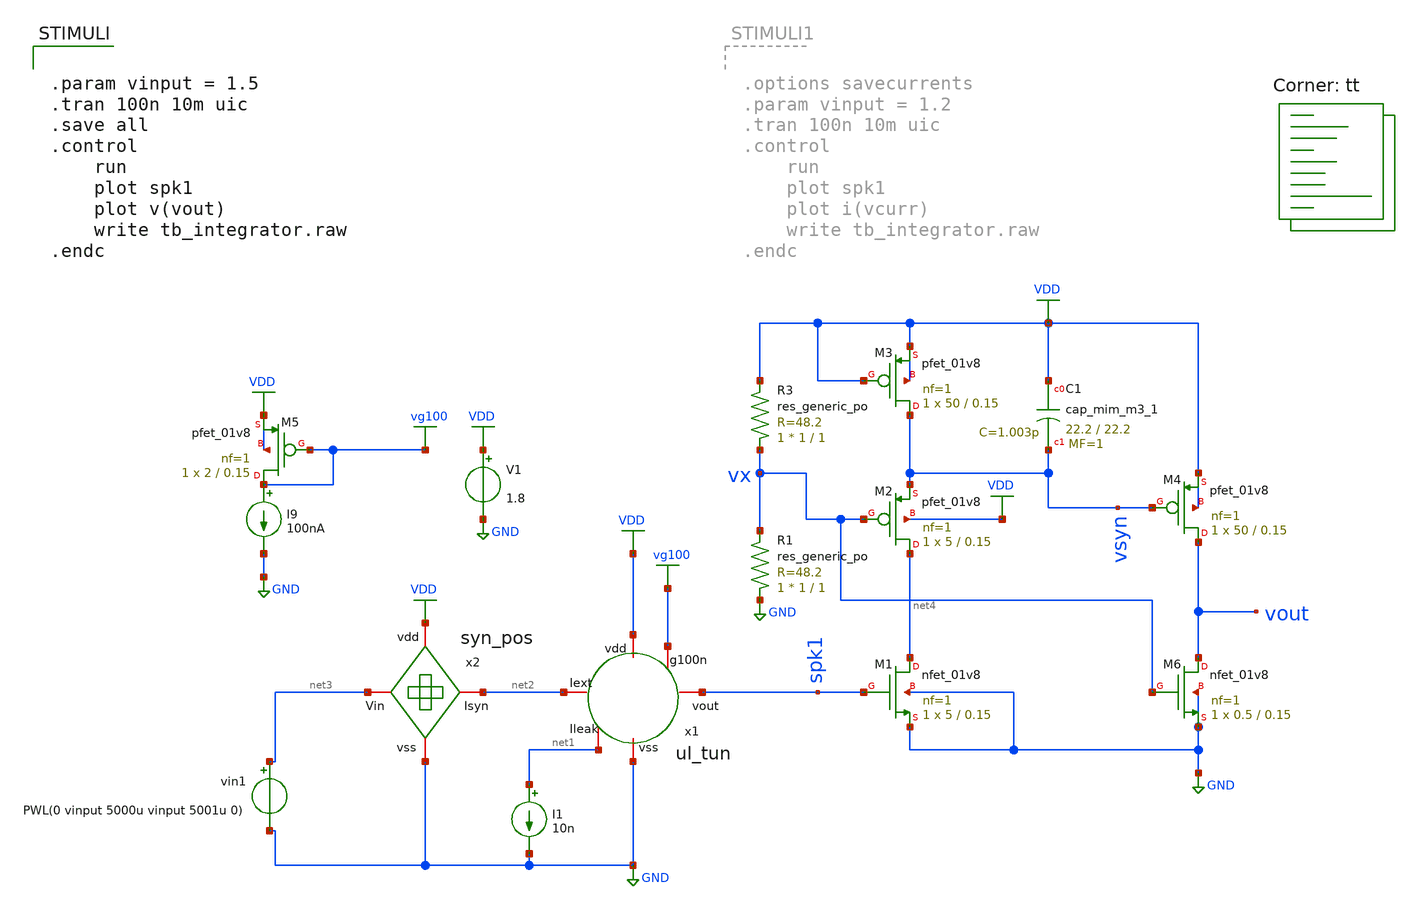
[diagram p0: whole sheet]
** sch_path: Neuron/ultralif/tb_integrator.sch
**.subckt tb_integrator
XM1 net4 spk1 GND GND sky130_fd_pr__nfet_01v8 L=0.15 W=5 nf=1 ad='int((nf+1)/2) * W/nf * 0.29' as='int((nf+2)/2) * W/nf * 0.29'
+ pd='2*int((nf+1)/2) * (W/nf + 0.29)' ps='2*int((nf+2)/2) * (W/nf + 0.29)' nrd='0.29 / W' nrs='0.29 / W'
+ sa=0 sb=0 sd=0 mult=1 m=1
XM2 net4 vx vsyn VDD sky130_fd_pr__pfet_01v8 L=0.15 W=5 nf=1 ad='int((nf+1)/2) * W/nf * 0.29' as='int((nf+2)/2) * W/nf * 0.29'
+ pd='2*int((nf+1)/2) * (W/nf + 0.29)' ps='2*int((nf+2)/2) * (W/nf + 0.29)' nrd='0.29 / W' nrs='0.29 / W'
+ sa=0 sb=0 sd=0 mult=1 m=1
XM3 vsyn VDD VDD VDD sky130_fd_pr__pfet_01v8 L=0.15 W=50 nf=1 ad='int((nf+1)/2) * W/nf * 0.29' as='int((nf+2)/2) * W/nf * 0.29'
+ pd='2*int((nf+1)/2) * (W/nf + 0.29)' ps='2*int((nf+2)/2) * (W/nf + 0.29)' nrd='0.29 / W' nrs='0.29 / W'
+ sa=0 sb=0 sd=0 mult=1 m=1
XM4 vout vsyn VDD VDD sky130_fd_pr__pfet_01v8 L=0.15 W=50 nf=1 ad='int((nf+1)/2) * W/nf * 0.29' as='int((nf+2)/2) * W/nf * 0.29'
+ pd='2*int((nf+1)/2) * (W/nf + 0.29)' ps='2*int((nf+2)/2) * (W/nf + 0.29)' nrd='0.29 / W' nrs='0.29 / W'
+ sa=0 sb=0 sd=0 mult=1 m=1
XC1 VDD vsyn sky130_fd_pr__cap_mim_m3_1 W=22.2 L=22.2 MF=1 m=1
V1 VDD GND 1.8
I1 net1 GND 10n
x1 net2 VDD vg100 spk1 net1 GND ul_tun
I9 vg100 GND 100nA
XM5 vg100 vg100 VDD VDD sky130_fd_pr__pfet_01v8 L=0.15 W=2 nf=1 ad='int((nf+1)/2) * W/nf * 0.29' as='int((nf+2)/2) * W/nf * 0.29'
+ pd='2*int((nf+1)/2) * (W/nf + 0.29)' ps='2*int((nf+2)/2) * (W/nf + 0.29)' nrd='0.29 / W' nrs='0.29 / W'
+ sa=0 sb=0 sd=0 mult=1 m=1
vin1 net3 GND PWL(0 vinput 5000u vinput 5001u 0)
x2 VDD net3 net2 GND syn_pos
XR3 vx VDD sky130_fd_pr__res_generic_po W=1 L=1 m=1
XR1 GND vx sky130_fd_pr__res_generic_po W=1 L=1 m=1
XM6 vout vx GND GND sky130_fd_pr__nfet_01v8 L=0.15 W=0.5 nf=1 ad='int((nf+1)/2) * W/nf * 0.29' as='int((nf+2)/2) * W/nf * 0.29'
+ pd='2*int((nf+1)/2) * (W/nf + 0.29)' ps='2*int((nf+2)/2) * (W/nf + 0.29)' nrd='0.29 / W' nrs='0.29 / W'
+ sa=0 sb=0 sd=0 mult=1 m=1
**** begin user architecture code
.lib $::SKYWATER_MODELS/sky130.lib.spice tt
**** end user architecture code
**.ends
.GLOBAL GND
.GLOBAL VDD
.GLOBAL vg100
**** begin user architecture code


.param vinput = 1.5
.tran 100n 10m uic
.save all
.control
	run
	plot spk1
	plot v(vout)
	write tb_integrator.raw
.endc


**** end user architecture code
.end
